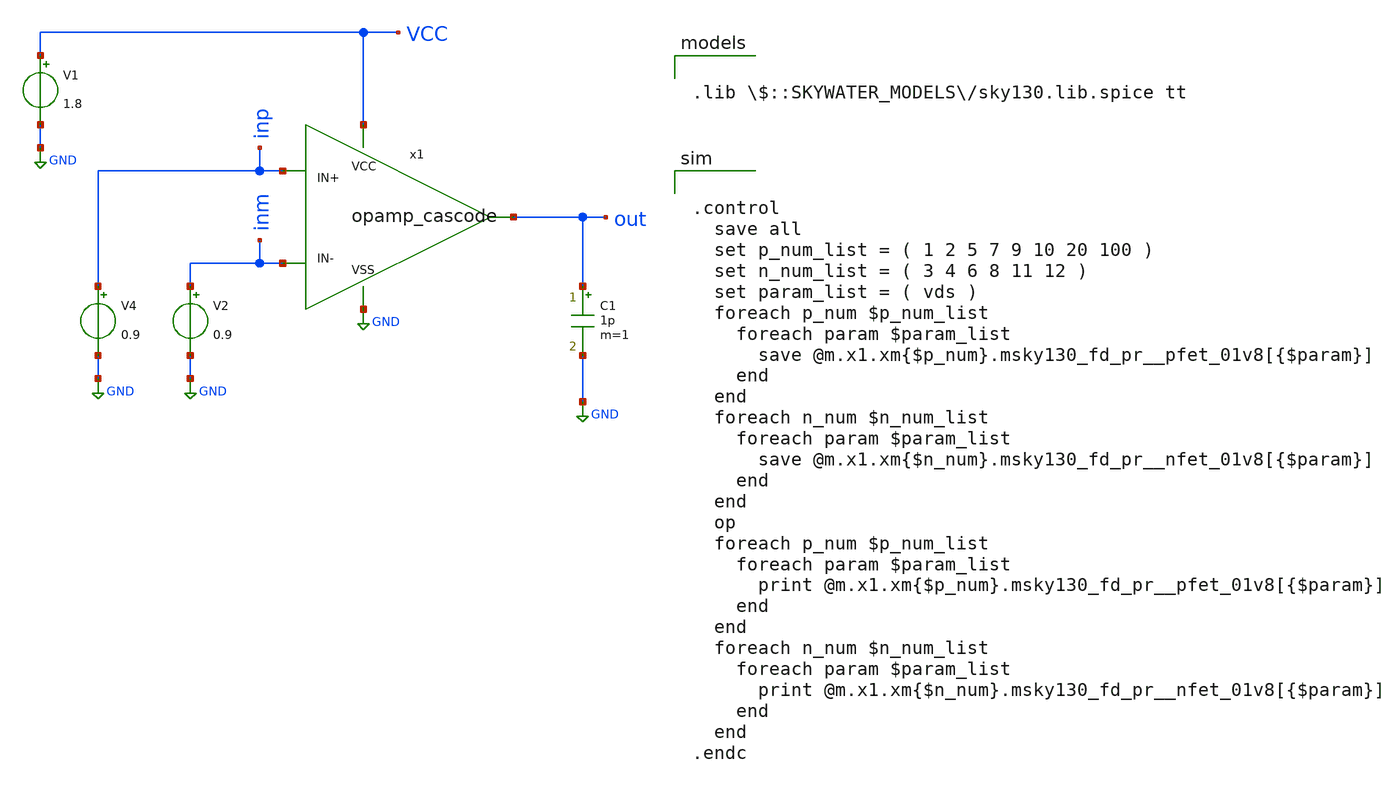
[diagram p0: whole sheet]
** sch_path: opamp_cascode_op_point.sch
**.subckt opamp_cascode_op_point
V1 VCC GND 1.8
V4 inp GND 0.9
V2 inm GND 0.9
C1 out GND 1p m=1
x1 VCC GND inp inm out opamp_cascode
**** begin user architecture code


.control
  save all
  set p_num_list = ( 1 2 5 7 9 10 20 100 )
  set n_num_list = ( 3 4 6 8 11 12 )
  set param_list = ( vds )
  foreach p_num $p_num_list
    foreach param $param_list
      save @m.x1.xm{$p_num}.msky130_fd_pr__pfet_01v8[{$param}]
    end
  end
  foreach n_num $n_num_list
    foreach param $param_list
      save @m.x1.xm{$n_num}.msky130_fd_pr__nfet_01v8[{$param}]
    end
  end
  op
  foreach p_num $p_num_list
    foreach param $param_list
      print @m.x1.xm{$p_num}.msky130_fd_pr__pfet_01v8[{$param}]
    end
  end
  foreach n_num $n_num_list
    foreach param $param_list
      print @m.x1.xm{$n_num}.msky130_fd_pr__nfet_01v8[{$param}]
    end
  end
.endc



.lib $::SKYWATER_MODELS/sky130.lib.spice tt

**** end user architecture code
**.ends

* expanding   symbol:  /home/zwierzak/projects/SKY130_OpAmp_GIT/opamp_cascode.sym # of pins=5
** sym_path: opamp_cascode.sym
** sch_path: opamp_cascode.sch
.subckt opamp_cascode VCC VSS IN+ IN- OUT
*.ipin IN+
*.ipin IN-
*.ipin VCC
*.ipin VSS
*.opin OUT
XM9 net8 net6 VCC VCC sky130_fd_pr__pfet_01v8 L=10 W=5 nf=1 ad='int((nf+1)/2) * W/nf * 0.29' as='int((nf+2)/2) * W/nf * 0.29'
+ pd='2*int((nf+1)/2) * (W/nf + 0.29)' ps='2*int((nf+2)/2) * (W/nf + 0.29)' nrd='0.29 / W' nrs='0.29 / W'
+ sa=0 sb=0 sd=0 mult=30 m=30
XM1 net7 net6 VCC VCC sky130_fd_pr__pfet_01v8 L=10 W=5 nf=1 ad='int((nf+1)/2) * W/nf * 0.29' as='int((nf+2)/2) * W/nf * 0.29'
+ pd='2*int((nf+1)/2) * (W/nf + 0.29)' ps='2*int((nf+2)/2) * (W/nf + 0.29)' nrd='0.29 / W' nrs='0.29 / W'
+ sa=0 sb=0 sd=0 mult=30 m=30
XM100 net3 net9 VCC VCC sky130_fd_pr__pfet_01v8 L=3 W=5 nf=1 ad='int((nf+1)/2) * W/nf * 0.29' as='int((nf+2)/2) * W/nf * 0.29'
+ pd='2*int((nf+1)/2) * (W/nf + 0.29)' ps='2*int((nf+2)/2) * (W/nf + 0.29)' nrd='0.29 / W' nrs='0.29 / W'
+ sa=0 sb=0 sd=0 mult=40 m=40
XM20 net9 net9 VCC VCC sky130_fd_pr__pfet_01v8 L=3 W=5 nf=1 ad='int((nf+1)/2) * W/nf * 0.29' as='int((nf+2)/2) * W/nf * 0.29'
+ pd='2*int((nf+1)/2) * (W/nf + 0.29)' ps='2*int((nf+2)/2) * (W/nf + 0.29)' nrd='0.29 / W' nrs='0.29 / W'
+ sa=0 sb=0 sd=0 mult=4 m=4
I0 net9 VSS 5.1u
XM10 OUT BIAS net8 net8 sky130_fd_pr__pfet_01v8 L=5 W=5 nf=1 ad='int((nf+1)/2) * W/nf * 0.29' as='int((nf+2)/2) * W/nf * 0.29'
+ pd='2*int((nf+1)/2) * (W/nf + 0.29)' ps='2*int((nf+2)/2) * (W/nf + 0.29)' nrd='0.29 / W' nrs='0.29 / W'
+ sa=0 sb=0 sd=0 mult=12 m=12
XM2 net6 BIAS net7 net7 sky130_fd_pr__pfet_01v8 L=5 W=5 nf=1 ad='int((nf+1)/2) * W/nf * 0.29' as='int((nf+2)/2) * W/nf * 0.29'
+ pd='2*int((nf+1)/2) * (W/nf + 0.29)' ps='2*int((nf+2)/2) * (W/nf + 0.29)' nrd='0.29 / W' nrs='0.29 / W'
+ sa=0 sb=0 sd=0 mult=12 m=12
XM5 net1 IN- net3 net3 sky130_fd_pr__pfet_01v8 L=0.18 W=5 nf=1 ad='int((nf+1)/2) * W/nf * 0.29' as='int((nf+2)/2) * W/nf * 0.29'
+ pd='2*int((nf+1)/2) * (W/nf + 0.29)' ps='2*int((nf+2)/2) * (W/nf + 0.29)' nrd='0.29 / W' nrs='0.29 / W'
+ sa=0 sb=0 sd=0 mult=50 m=50
XM7 net2 IN+ net3 net3 sky130_fd_pr__pfet_01v8 L=0.18 W=5 nf=1 ad='int((nf+1)/2) * W/nf * 0.29' as='int((nf+2)/2) * W/nf * 0.29'
+ pd='2*int((nf+1)/2) * (W/nf + 0.29)' ps='2*int((nf+2)/2) * (W/nf + 0.29)' nrd='0.29 / W' nrs='0.29 / W'
+ sa=0 sb=0 sd=0 mult=50 m=50
XM6 net1 net1 VSS VSS sky130_fd_pr__nfet_01v8 L=1 W=5 nf=1 ad='int((nf+1)/2) * W/nf * 0.29' as='int((nf+2)/2) * W/nf * 0.29'
+ pd='2*int((nf+1)/2) * (W/nf + 0.29)' ps='2*int((nf+2)/2) * (W/nf + 0.29)' nrd='0.29 / W' nrs='0.29 / W'
+ sa=0 sb=0 sd=0 mult=3 m=3
XM8 net2 net2 VSS VSS sky130_fd_pr__nfet_01v8 L=1 W=5 nf=1 ad='int((nf+1)/2) * W/nf * 0.29' as='int((nf+2)/2) * W/nf * 0.29'
+ pd='2*int((nf+1)/2) * (W/nf + 0.29)' ps='2*int((nf+2)/2) * (W/nf + 0.29)' nrd='0.29 / W' nrs='0.29 / W'
+ sa=0 sb=0 sd=0 mult=3 m=3
XM12 net4 net2 VSS VSS sky130_fd_pr__nfet_01v8 L=1 W=5 nf=1 ad='int((nf+1)/2) * W/nf * 0.29' as='int((nf+2)/2) * W/nf * 0.29'
+ pd='2*int((nf+1)/2) * (W/nf + 0.29)' ps='2*int((nf+2)/2) * (W/nf + 0.29)' nrd='0.29 / W' nrs='0.29 / W'
+ sa=0 sb=0 sd=0 mult=6 m=6
XM4 net5 net1 VSS VSS sky130_fd_pr__nfet_01v8 L=1 W=5 nf=1 ad='int((nf+1)/2) * W/nf * 0.29' as='int((nf+2)/2) * W/nf * 0.29'
+ pd='2*int((nf+1)/2) * (W/nf + 0.29)' ps='2*int((nf+2)/2) * (W/nf + 0.29)' nrd='0.29 / W' nrs='0.29 / W'
+ sa=0 sb=0 sd=0 mult=6 m=6
XM11 OUT BIAS1 net4 net4 sky130_fd_pr__nfet_01v8 L=3 W=5 nf=1 ad='int((nf+1)/2) * W/nf * 0.29' as='int((nf+2)/2) * W/nf * 0.29'
+ pd='2*int((nf+1)/2) * (W/nf + 0.29)' ps='2*int((nf+2)/2) * (W/nf + 0.29)' nrd='0.29 / W' nrs='0.29 / W'
+ sa=0 sb=0 sd=0 mult=9 m=9
XM3 net6 BIAS1 net5 net5 sky130_fd_pr__nfet_01v8 L=3 W=5 nf=1 ad='int((nf+1)/2) * W/nf * 0.29' as='int((nf+2)/2) * W/nf * 0.29'
+ pd='2*int((nf+1)/2) * (W/nf + 0.29)' ps='2*int((nf+2)/2) * (W/nf + 0.29)' nrd='0.29 / W' nrs='0.29 / W'
+ sa=0 sb=0 sd=0 mult=9 m=9
V1 BIAS VSS 0
V2 BIAS1 VSS 0.9
C1 net6 VSS 400f m=1
.ends

.GLOBAL GND
.end
